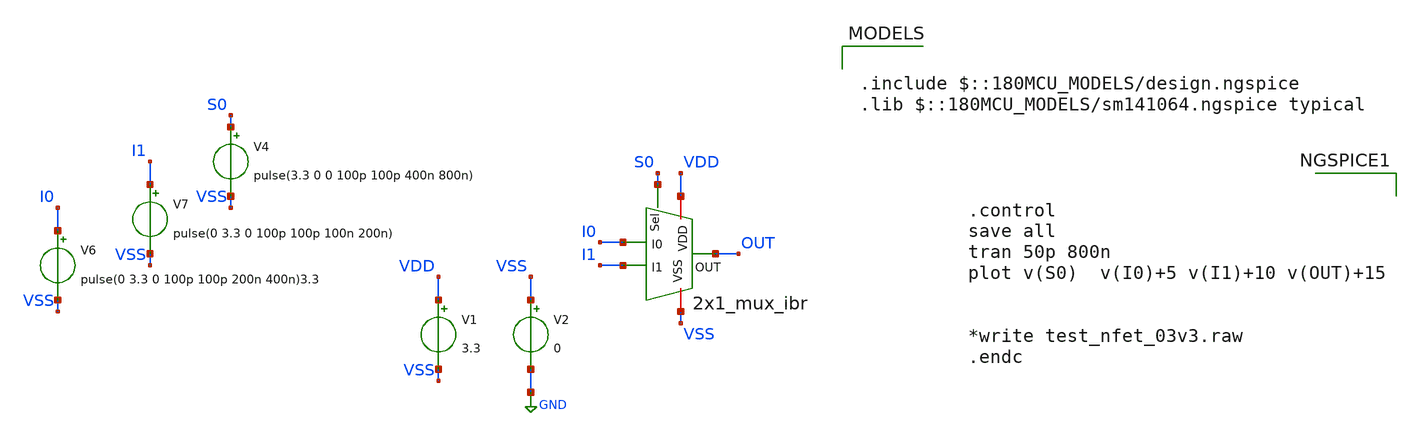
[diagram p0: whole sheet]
** sch_path: Clock_Generator_PAKISTAN_02/Schematics/2x1_mux_test_ibr..sch
**.subckt 2x1_mux_test_ibr.
V1 VDD VSS 3.3
V2 VSS GND 0
V4 S0 VSS pulse(3.3 0 0 100p 100p 400n 800n)
V6 I0 VSS pulse(0 3.3 0 100p 100p 200n 400n)3.3
V7 I1 VSS pulse(0 3.3 0 100p 100p 100n 200n)
x1 VSS S0 OUT I0 I1 VDD 2x1_mux_ibr
**** begin user architecture code

.include $::180MCU_MODELS/design.ngspice
.lib $::180MCU_MODELS/sm141064.ngspice typical



.control
save all
tran 50p 800n
plot v(S0)  v(I0)+5 v(I1)+10 v(OUT)+15


*write test_nfet_03v3.raw
.endc


**** end user architecture code
**.ends
.GLOBAL GND
.end
